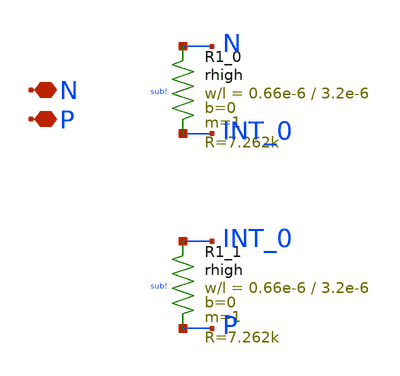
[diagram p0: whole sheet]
** sch_path: design/LELO_TR_IHP13G2/LELOTR_RES2.sch
**.subckt LELOTR_RES2 N P
*.iopin N
*.iopin P
XR1_0 N INT_0 sub! rhigh w=0.66e-6 l=3.2e-6 m=1 b=0 mm_ok=1
XR1_1 INT_0 P sub! rhigh w=0.66e-6 l=3.2e-6 m=1 b=0 mm_ok=1
**.ends
.end
